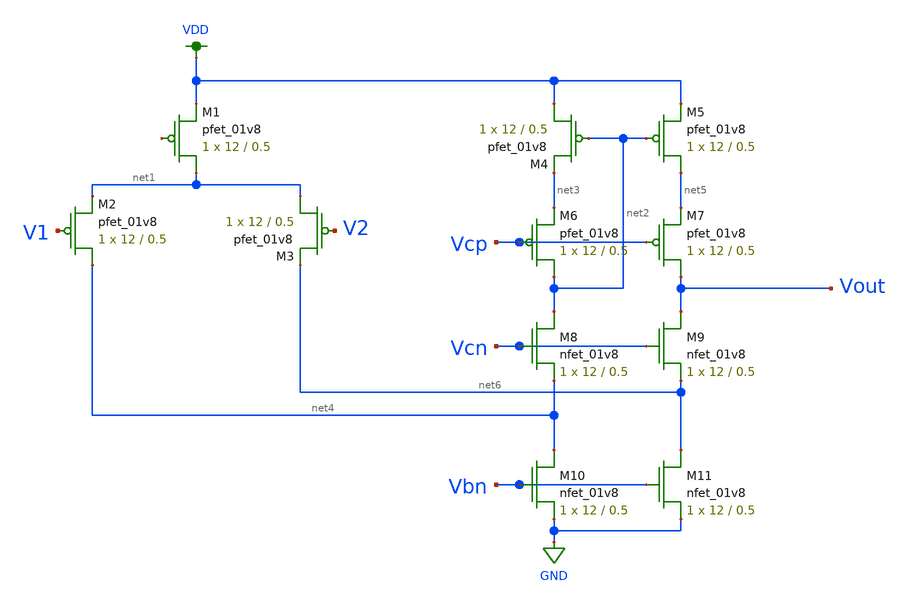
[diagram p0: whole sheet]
** sch_path: MP3/cascode.sch
**.subckt cascode
XM1 net1 net7 VDD VDD sky130_fd_pr__pfet_01v8 L=0.5 W=12 nf=1 ad='int((nf+1)/2) * W/nf * 0.29' as='int((nf+2)/2) * W/nf * 0.29'
+ pd='2*int((nf+1)/2) * (W/nf + 0.29)' ps='2*int((nf+2)/2) * (W/nf + 0.29)' nrd='0.29 / W' nrs='0.29 / W'
+ sa=0 sb=0 sd=0 mult=1 m=1
XM2 net4 V1 net1 VDD sky130_fd_pr__pfet_01v8 L=0.5 W=12 nf=1 ad='int((nf+1)/2) * W/nf * 0.29' as='int((nf+2)/2) * W/nf * 0.29'
+ pd='2*int((nf+1)/2) * (W/nf + 0.29)' ps='2*int((nf+2)/2) * (W/nf + 0.29)' nrd='0.29 / W' nrs='0.29 / W'
+ sa=0 sb=0 sd=0 mult=1 m=1
XM3 net1 V2 net6 VDD sky130_fd_pr__pfet_01v8 L=0.5 W=12 nf=1 ad='int((nf+1)/2) * W/nf * 0.29' as='int((nf+2)/2) * W/nf * 0.29'
+ pd='2*int((nf+1)/2) * (W/nf + 0.29)' ps='2*int((nf+2)/2) * (W/nf + 0.29)' nrd='0.29 / W' nrs='0.29 / W'
+ sa=0 sb=0 sd=0 mult=1 m=1
XM4 VDD net2 net3 VDD sky130_fd_pr__pfet_01v8 L=0.5 W=12 nf=1 ad='int((nf+1)/2) * W/nf * 0.29' as='int((nf+2)/2) * W/nf * 0.29'
+ pd='2*int((nf+1)/2) * (W/nf + 0.29)' ps='2*int((nf+2)/2) * (W/nf + 0.29)' nrd='0.29 / W' nrs='0.29 / W'
+ sa=0 sb=0 sd=0 mult=1 m=1
XM5 net5 net2 VDD VDD sky130_fd_pr__pfet_01v8 L=0.5 W=12 nf=1 ad='int((nf+1)/2) * W/nf * 0.29' as='int((nf+2)/2) * W/nf * 0.29'
+ pd='2*int((nf+1)/2) * (W/nf + 0.29)' ps='2*int((nf+2)/2) * (W/nf + 0.29)' nrd='0.29 / W' nrs='0.29 / W'
+ sa=0 sb=0 sd=0 mult=1 m=1
XM6 net2 Vcp net3 VDD sky130_fd_pr__pfet_01v8 L=0.5 W=12 nf=1 ad='int((nf+1)/2) * W/nf * 0.29' as='int((nf+2)/2) * W/nf * 0.29'
+ pd='2*int((nf+1)/2) * (W/nf + 0.29)' ps='2*int((nf+2)/2) * (W/nf + 0.29)' nrd='0.29 / W' nrs='0.29 / W'
+ sa=0 sb=0 sd=0 mult=1 m=1
XM7 Vout Vcp net5 VDD sky130_fd_pr__pfet_01v8 L=0.5 W=12 nf=1 ad='int((nf+1)/2) * W/nf * 0.29' as='int((nf+2)/2) * W/nf * 0.29'
+ pd='2*int((nf+1)/2) * (W/nf + 0.29)' ps='2*int((nf+2)/2) * (W/nf + 0.29)' nrd='0.29 / W' nrs='0.29 / W'
+ sa=0 sb=0 sd=0 mult=1 m=1
XM8 net2 Vcn net4 GND sky130_fd_pr__nfet_01v8 L=0.5 W=12 nf=1 ad='int((nf+1)/2) * W/nf * 0.29' as='int((nf+2)/2) * W/nf * 0.29'
+ pd='2*int((nf+1)/2) * (W/nf + 0.29)' ps='2*int((nf+2)/2) * (W/nf + 0.29)' nrd='0.29 / W' nrs='0.29 / W'
+ sa=0 sb=0 sd=0 mult=1 m=1
XM9 Vout Vcn net6 GND sky130_fd_pr__nfet_01v8 L=0.5 W=12 nf=1 ad='int((nf+1)/2) * W/nf * 0.29' as='int((nf+2)/2) * W/nf * 0.29'
+ pd='2*int((nf+1)/2) * (W/nf + 0.29)' ps='2*int((nf+2)/2) * (W/nf + 0.29)' nrd='0.29 / W' nrs='0.29 / W'
+ sa=0 sb=0 sd=0 mult=1 m=1
XM10 net4 Vbn GND GND sky130_fd_pr__nfet_01v8 L=0.5 W=12 nf=1 ad='int((nf+1)/2) * W/nf * 0.29' as='int((nf+2)/2) * W/nf * 0.29'
+ pd='2*int((nf+1)/2) * (W/nf + 0.29)' ps='2*int((nf+2)/2) * (W/nf + 0.29)' nrd='0.29 / W' nrs='0.29 / W'
+ sa=0 sb=0 sd=0 mult=1 m=1
XM11 net6 Vbn GND GND sky130_fd_pr__nfet_01v8 L=0.5 W=12 nf=1 ad='int((nf+1)/2) * W/nf * 0.29' as='int((nf+2)/2) * W/nf * 0.29'
+ pd='2*int((nf+1)/2) * (W/nf + 0.29)' ps='2*int((nf+2)/2) * (W/nf + 0.29)' nrd='0.29 / W' nrs='0.29 / W'
+ sa=0 sb=0 sd=0 mult=1 m=1
**.ends
.GLOBAL VDD
.GLOBAL GND
.end
